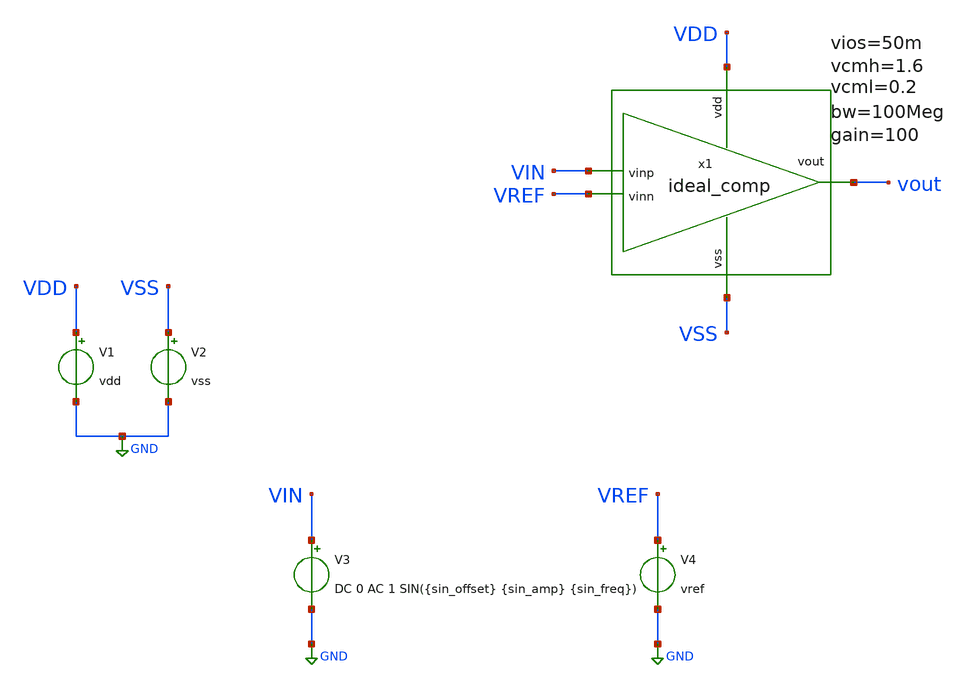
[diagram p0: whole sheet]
** sch_path: simulation/tb_comp.sch
**.subckt tb_comp
V1 VDD GND vdd
V2 VSS GND vss
V3 VIN GND DC 0 AC 1 SIN({sin_offset} {sin_amp} {sin_freq})
V4 VREF GND vref
x1 VDD VSS VIN vout VREF ideal_comp bw=100Meg gain=100 vdd= vss= vin_h= vin_l= vios=50m
**** begin user architecture code



# Model files
.lib /usr/local/share/pdk/sky130A/libs.tech/ngspice/sky130.lib.spice tt

# Main parameters
.param vdd=1.8 vss=0 vref='vdd/2' vhigh=1.8 vlow=0
.param sin_offset='vdd/2'
.param sin_amp='vdd/2'
.param sin_freq=10Meg
.param sin_period='1/sin_freq'
.param tran_step='sin_period/10'
.param tran_stop_time='sin_period*2'

# Component parameters



# Save settings
.save all


# Analysis
.op
.tran {tran_step} {tran_stop_time}

# Start control block
.control

# Run sim
run

# Expressions

# Save expressions

# Write to raw file
write tb_comp_top.raw
# wrdata custom_output.txt



.endc



**** end user architecture code
**.ends

* expanding   symbol:  /home/nwells/xschem/6_bit_flash/schematics/ideal_comp.sym # of pins=5
** sym_path: schematics/ideal_comp.sym
** sch_path: schematics/ideal_comp.sch
.subckt ideal_comp vdd vss vinp vout vinn  bw=100Meg gain=100 vcmh=1.6 vcml=0.2 vios=50m
*.ipin vdd
*.opin vout
*.ipin vss
*.ipin vinp
*.ipin vinn
B1 vp vss V = {V(vinp)<vcmh ? (V(vinp) < vcml ? vcml: V(vinp)) : vcmh}
B2 vn vss V = {V(vinn)<vcmh ? (V(vinn) < vcml ? vcml: V(vinn) + vios) : vcmh}
B3 net1 vss V = {gain*(V(vp)-V(vn)) < V(vdd) ? (gain*(V(vp)-V(vn)) < V(vss) ? V(vss) : (gain*(V(vp)-V(vn)))) : V(vdd)}
R1 vout net1 {1/(2*3.1415*bw*1p)} m=1
C1 vout vss 1p m=1
.ends

.GLOBAL GND
.end
